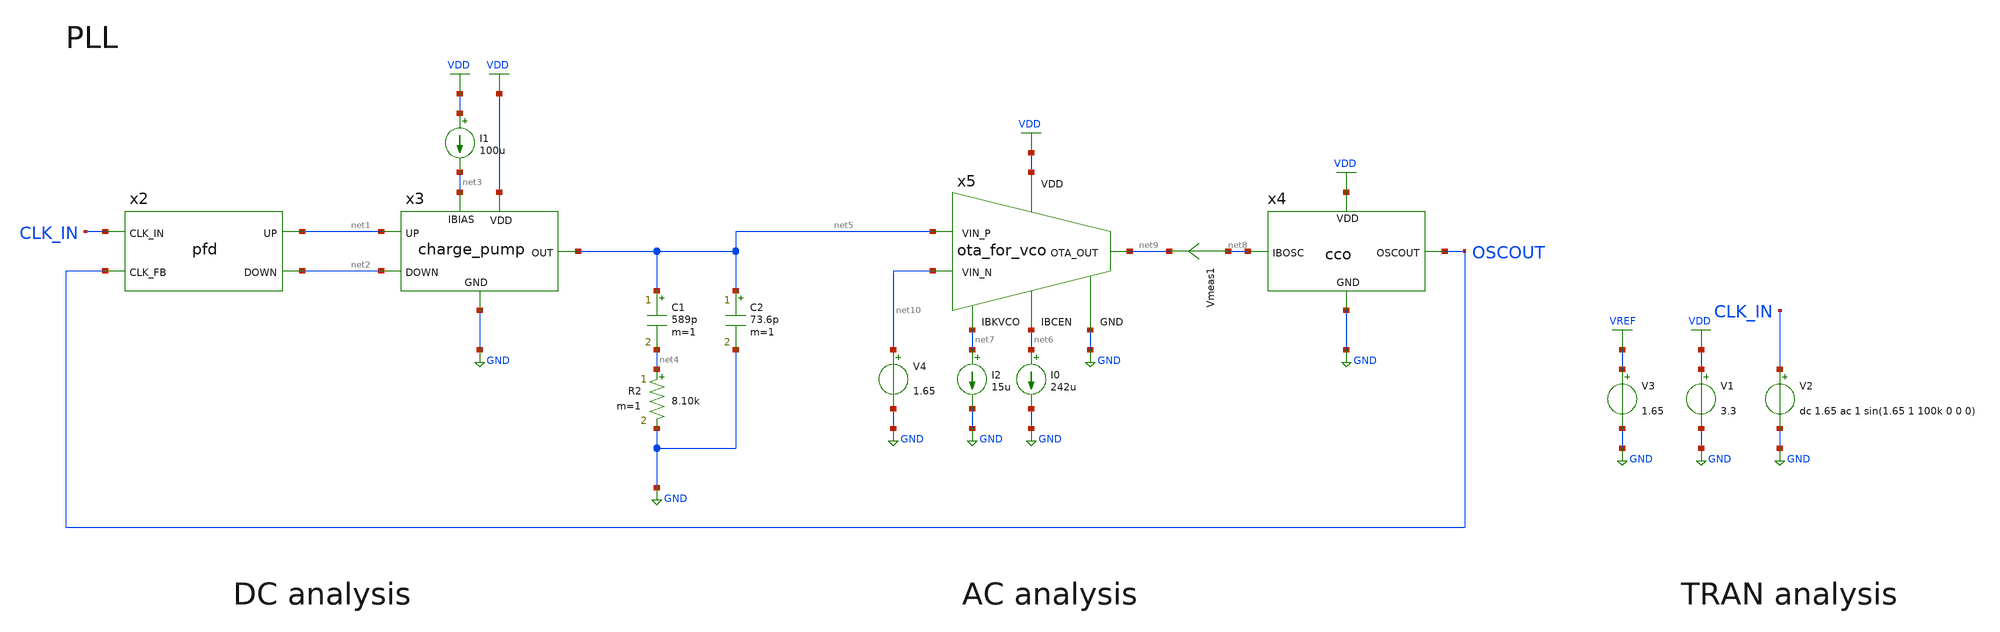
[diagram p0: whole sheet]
** sch_path: designs/libs/tb_analog/tb_pll/tb_pll.sch
* Copyright 2022 GlobalFoundries PDK Authors
* Licensed under the Apache License, Version 2.0 (the "License");
* you may not use this file except in compliance with the License.
* You may obtain a copy of the License at
* https://www.apache.org/licenses/LICENSE-2.0
* Unless required by applicable law or agreed to in writing, software
* distributed under the License is distributed on an "AS IS" BASIS,
* WITHOUT WARRANTIES OR CONDITIONS OF ANY KIND, either express or implied.
* See the License for the specific language governing permissions and
* limitations under the License.
**.subckt tb_pll
V1 VDD GND 3.3
I1 VDD net3 100u
V2 CLK_IN GND dc 1.65 ac 1 sin(1.65 1 100k 0 0 0)
V3 VREF GND 1.65
x2 net1 CLK_IN OSCOUT net2 pfd
x3 VDD GND net1 net2 net5 net3 charge_pump
R2 net4 GND 8.10k m=1
C1 net5 net4 589p m=1
C2 net5 GND 73.6p m=1
I0 net6 GND 242u
x4 VDD GND net8 OSCOUT cco
x5 net7 net10 net5 net9 GND VDD net6 ota_for_vco
I2 net7 GND 15u
Vmeas1 net8 net9 0
.save i(vmeas1)
V4 net10 GND 1.65
**** begin user architecture code

.control
save all
save currents
* DC analysis
dc v2 0 3.3 0.1 rload 10k 100k 20k
* let dc_gain=deriv(vout)
write tb_pll_dc.raw
* AC analysis
ac dec 10 1k 10Meg
let ac_gain = vout / vin_p
let ac_gain_db = db(ac_gain)
let ac_phase_deg = (180 / PI) * cph(ac_gain)
write tb_pll_ac.raw
* TRAN analysis
tran 0.1u 100u
write tb_pll_tran.raw
.endc



.include $::180MCU_MODELS/design.ngspice
.lib $::180MCU_MODELS/sm141064.ngspice typical
.lib $::180MCU_MODELS/sm141064.ngspice cap_mim
.lib $::180MCU_MODELS/sm141064.ngspice res_typical
.lib $::180MCU_MODELS/sm141064.ngspice moscap_typical
.lib $::180MCU_MODELS/sm141064.ngspice mimcap_typical
* .lib $::180MCU_MODELS/sm141064.ngspice res_statistical

**** end user architecture code
**.ends
.GLOBAL VDD
.GLOBAL GND
.GLOBAL VREF
.end
